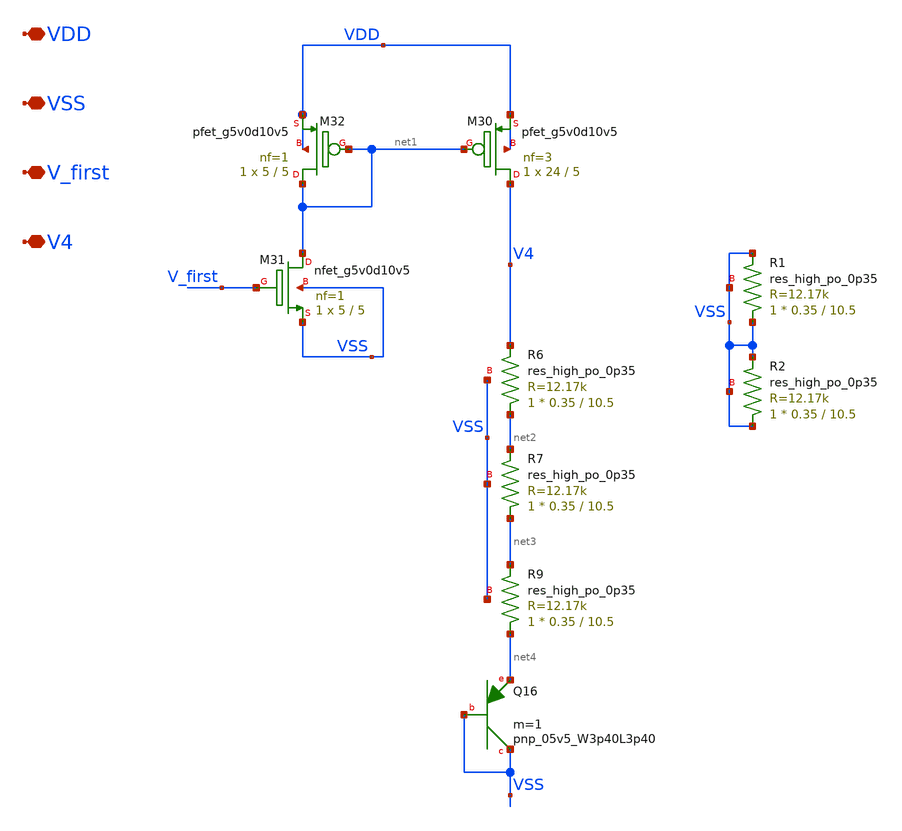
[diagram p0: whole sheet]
** sch_path: xschem/xschem_BGR_Top/BGR_2nd_parta.sch
**.subckt BGR_2nd_parta VDD VSS V_first V4
*.iopin VDD
*.iopin VSS
*.iopin V_first
*.iopin V4
XQ16 VSS VSS net4 sky130_fd_pr__pnp_05v5_W3p40L3p40 m=1
XM30 V4 net1 VDD VDD sky130_fd_pr__pfet_g5v0d10v5 L=5 W=24 nf=3 ad='int((nf+1)/2) * W/nf * 0.29' as='int((nf+2)/2) * W/nf * 0.29'
+ pd='2*int((nf+1)/2) * (W/nf + 0.29)' ps='2*int((nf+2)/2) * (W/nf + 0.29)' nrd='0.29 / W' nrs='0.29 / W'
+ sa=0 sb=0 sd=0 mult=1 m=1
XM31 net1 V_first VSS VSS sky130_fd_pr__nfet_g5v0d10v5 L=5 W=5 nf=1 ad='int((nf+1)/2) * W/nf * 0.29'
+ as='int((nf+2)/2) * W/nf * 0.29' pd='2*int((nf+1)/2) * (W/nf + 0.29)' ps='2*int((nf+2)/2) * (W/nf + 0.29)'
+ nrd='0.29 / W' nrs='0.29 / W' sa=0 sb=0 sd=0 mult=1 m=1
XM32 net1 net1 VDD VDD sky130_fd_pr__pfet_g5v0d10v5 L=5 W=5 nf=1 ad='int((nf+1)/2) * W/nf * 0.29' as='int((nf+2)/2) * W/nf * 0.29'
+ pd='2*int((nf+1)/2) * (W/nf + 0.29)' ps='2*int((nf+2)/2) * (W/nf + 0.29)' nrd='0.29 / W' nrs='0.29 / W'
+ sa=0 sb=0 sd=0 mult=1 m=1
XR6 net2 V4 VSS sky130_fd_pr__res_high_po_0p35 L=10.5 mult=1 m=1
XR7 net3 net2 VSS sky130_fd_pr__res_high_po_0p35 L=10.5 mult=1 m=1
XR9 net4 net3 VSS sky130_fd_pr__res_high_po_0p35 L=10.5 mult=1 m=1
XR1 VSS VSS VSS sky130_fd_pr__res_high_po_0p35 L=10.5 mult=1 m=1
XR2 VSS VSS VSS sky130_fd_pr__res_high_po_0p35 L=10.5 mult=1 m=1
**.ends
.end
